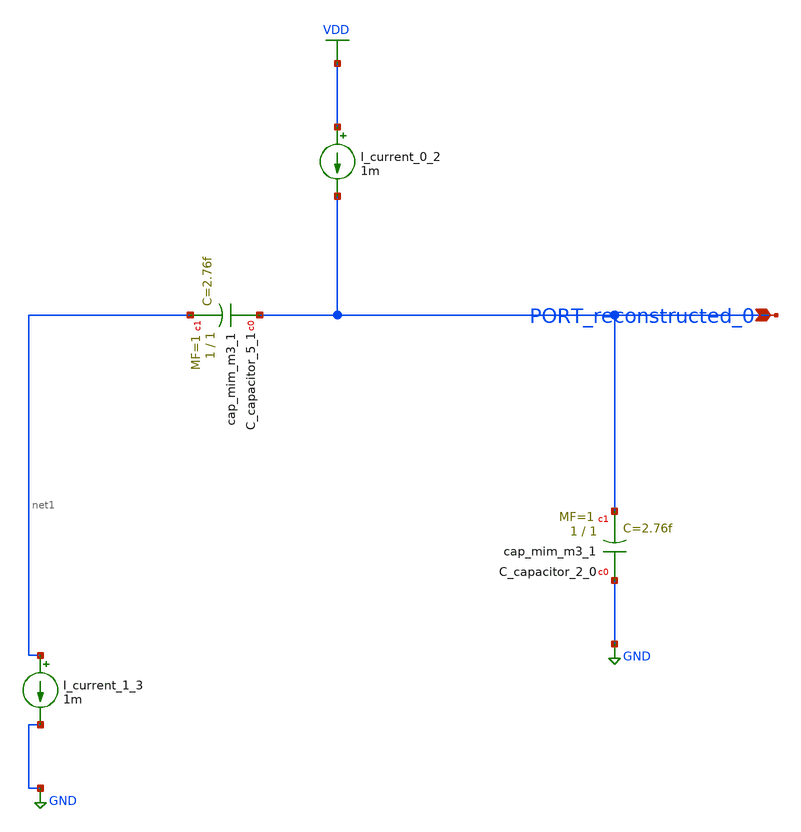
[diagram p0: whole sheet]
** sch_path: schematics/AMSNet/734.sch
**.subckt 734 PORT_reconstructed_0
*.ipin PORT_reconstructed_0
XC_capacitor_2_0 GND PORT_reconstructed_0 sky130_fd_pr__cap_mim_m3_1 W=1 L=1 MF=1 m=1
XC_capacitor_5_1 PORT_reconstructed_0 net1 sky130_fd_pr__cap_mim_m3_1 W=1 L=1 MF=1 m=1
I_current_0_2 VDD PORT_reconstructed_0 1m
I_current_1_3 net1 GND 1m
**.ends
.GLOBAL GND
.GLOBAL VDD
.end
